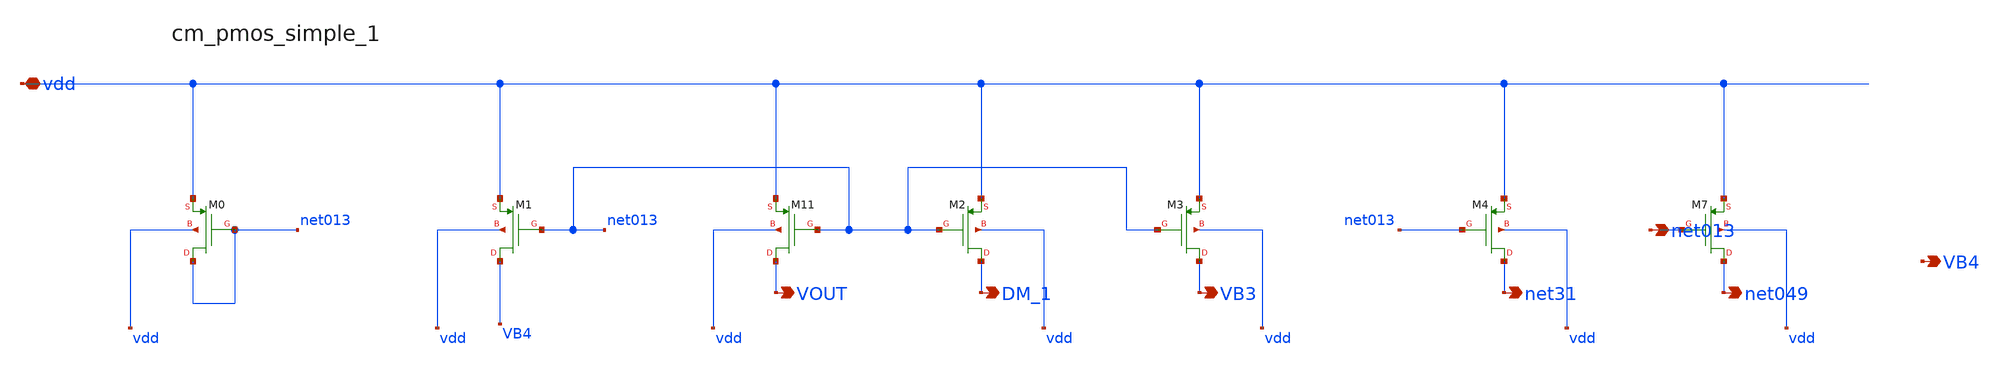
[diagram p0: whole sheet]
** sch_path: analog-db/raw/amp_009_leung_nmcnr/hier/blocks/cm_pmos_simple_1.sch
**.subckt cm_pmos_simple_1 vdd net013 VOUT DM_1 VB3 net31 net049 VB4
*.iopin vdd
*.opin net013
*.opin VOUT
*.opin DM_1
*.opin VB3
*.opin net31
*.opin net049
*.opin VB4
XM0 net013 net013 vdd vdd sg13_lv_pmos w=x_dut_xm0_w l=x_dut_xm0_l ng=1 m=x_dut_xm0_m
XM1 VB4 net013 vdd vdd sg13_lv_pmos w=x_dut_xm1_w l=x_dut_xm1_l ng=1 m=x_dut_xm1_m
XM11 VOUT net013 vdd vdd sg13_lv_pmos w=x_dut_xm11_w l=x_dut_xm11_l ng=1 m=x_dut_xm11_m
XM2 DM_1 net013 vdd vdd sg13_lv_pmos w=x_dut_xm2_w l=x_dut_xm2_l ng=1 m=x_dut_xm2_m
XM3 VB3 net013 vdd vdd sg13_lv_pmos w=x_dut_xm3_w l=x_dut_xm3_l ng=1 m=x_dut_xm3_m
XM4 net31 net013 vdd vdd sg13_lv_pmos w=x_dut_xm4_w l=x_dut_xm4_l ng=1 m=x_dut_xm4_m
XM7 net049 net013 vdd vdd sg13_lv_pmos w=x_dut_xm7_w l=x_dut_xm7_l ng=1 m=x_dut_xm7_m
**.ends
.end
